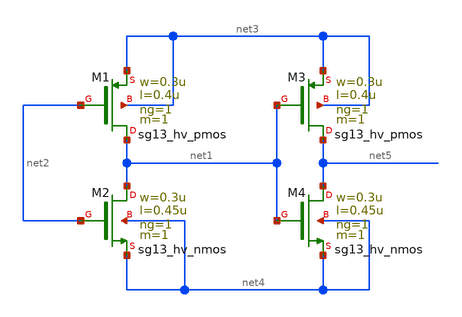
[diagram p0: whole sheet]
** sch_path: schematics/misc/buffer_hv.sch
**.subckt buffer_hv
XM1 net1 net2 net3 net3 sg13_hv_pmos w=0.3u l=0.4u ng=1 m=1 mm_ok=1
XM2 net1 net2 net4 net4 sg13_hv_nmos w=0.3u l=0.45u ng=1 m=1 mm_ok=1
XM3 net5 net1 net3 net3 sg13_hv_pmos w=0.3u l=0.4u ng=1 m=1 mm_ok=1
XM4 net5 net1 net4 net4 sg13_hv_nmos w=0.3u l=0.45u ng=1 m=1 mm_ok=1
**.ends
.end
